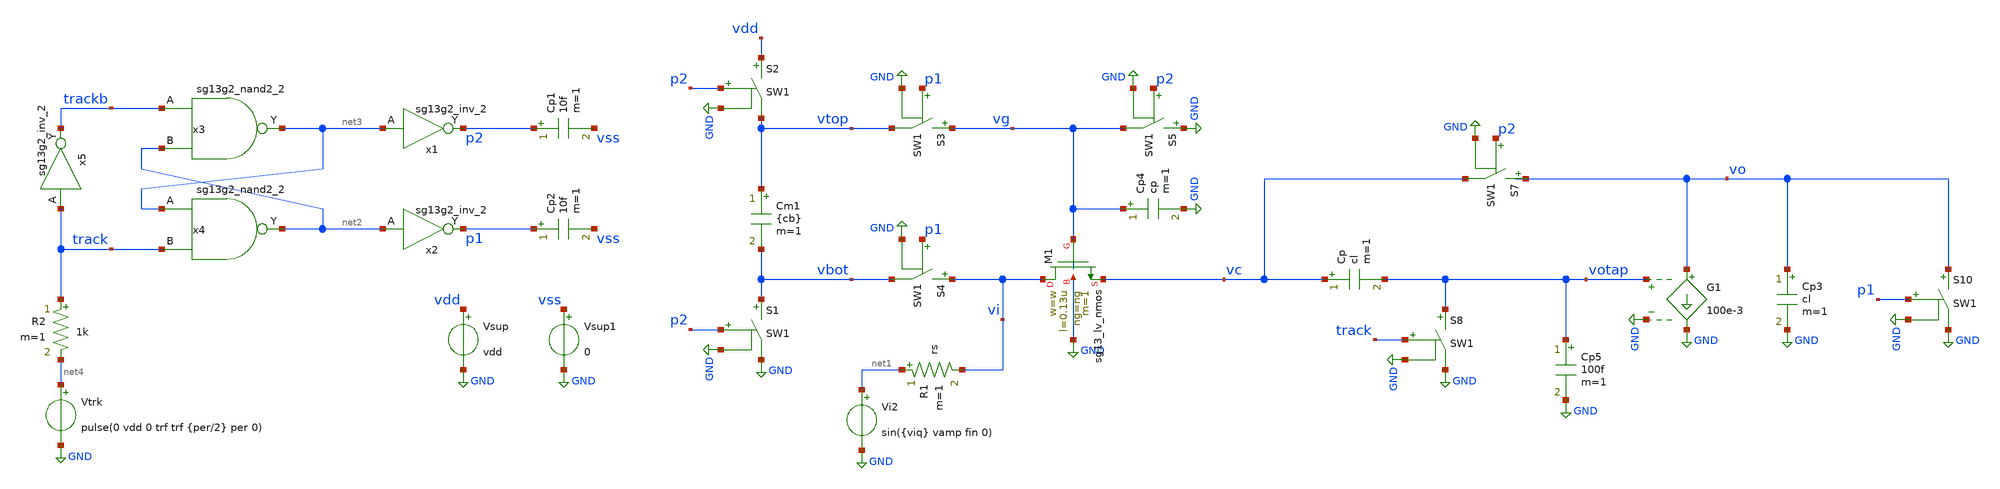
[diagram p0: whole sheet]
** sch_path: xschem/tb_boot_bottom.sch
* IHP-GmbH/IHP-Open-PDK/ihp-sg13g2/libs.tech/xschem/sg13g2_stdcells/sg13g2_inv_2.sch:
* Copyright 2023 IHP PDK Authors
* Licensed under the Apache License, Version 2.0 (the "License");
**.subckt tb_boot_bottom
Cm1 vtop vbot {cb} m=1
S1 vbot GND p2 GND SW1
S2 vdd vtop p2 GND SW1
S3 vg vtop p1 GND SW1
S4 vi vbot p1 GND SW1
S5 GND vg p2 GND SW1
Cp4 vg GND cp m=1
Vi2 net1 GND sin({viq} vamp fin 0)
Cp1 p2 vss 10f m=1
Cp2 p1 vss 10f m=1
x1 p2 net3 VDD VSS sg13g2_inv_2
x2 p1 net2 VDD VSS sg13g2_inv_2
x3 net3 trackb net2 VDD VSS sg13g2_nand2_2
x4 net2 net3 track VDD VSS sg13g2_nand2_2
x5 trackb track VDD VSS sg13g2_inv_2
Vtrk net4 GND pulse(0 vdd 0 trf trf {per/2} per 0)
Vsup vdd GND vdd
Vsup1 vss GND 0
R1 net1 vi rs m=1
XM1 vi vg vc GND sg13_lv_nmos w=w l=0.13u ng=ng m=1 mm_ok=1
Cp vc votap cl m=1
G1 vo GND votap GND 100e-3
S7 vo vc p2 GND SW1
Cp3 vo GND cl m=1
S8 votap GND track GND SW1
S10 vo GND p1 GND SW1
Cp5 votap GND 100f m=1
R2 track net4 1k m=1
**** begin user architecture code


.lib cornerMOSlv.lib mos_tt
.inc /foss/pdks/ihp-sg13g2/libs.ref/sg13g2_stdcell/spice/sg13g2_stdcell.spice
.param vdd=1.2 viq=0.3 vamp=0.2
.param cl=1p cb=1p cp=100f w=100u ng=20
.param ndft=31 npad=5 bin=5 fclk=500e6 runs=15
.param per=1/fclk fin=fclk*bin/ndft trf=100p
.param vh=0 rsw=10 roff=1e9 rs=10

.csparam per=per runs=runs
.csparam tstop1 = 4*per
.csparam tstop2 = per*(ndft+npad)
.option method=gear reltol=1e-6 chgtol=1e-16

.control
    tran 1n $&tstop1
    write tb_boot_bottom.raw
    option numdgt=9
    set wr_singlescale
    set wr_vecnames
    compose bin_vec start=1 stop=$&runs step=1
    foreach i $&bin_vec
      alterparam bin=$i
      reset
      tran 10p $&tstop2 0
      let lin-tstep = per
      let lin-tstart = 1.1n
      linearize
      wrdata tb_boot_bottom_track.txt v(vi) v(vc)
      tran 10p $&tstop2 0
      let lin-tstep = per
      let lin-tstart = 1.9n
      linearize
      wrdata tb_boot_bottom.txt v(vi) v(vo)
      destroy all
      set appendwrite
      unset wr_vecnames
    end
    unset appendwrite
.endc


**** end user architecture code
**.ends

* expanding   symbol:  sg13g2_stdcells/sg13g2_inv_2.sym # of pins=2
** sym_path: sg13g2_stdcells/sg13g2_inv_2.sym
** sch_path: sg13g2_stdcells/sg13g2_inv_2.sch
.subckt sg13g2_inv_2 Y A VDD VSS
*.opin Y
*.ipin A
*.iopin VDD
*.iopin VSS
XM1 Y A VSS VSS sg13_lv_nmos w=1.48u l=130.00n ng=2 m=1 mm_ok=1
XM2 Y A VDD VDD sg13_lv_pmos w=2.24u l=130.00n ng=2 m=1 mm_ok=1
.ends


* expanding   symbol:  sg13g2_stdcells/sg13g2_nand2_2.sym # of pins=3
** sym_path: sg13g2_stdcells/sg13g2_nand2_2.sym
** sch_path: sg13g2_stdcells/sg13g2_nand2_2.sch
.subckt sg13g2_nand2_2 Y A B VDD VSS
*.iopin VDD
*.iopin VSS
*.opin Y
*.ipin B
*.ipin A
XM1 Y A net1 VSS sg13_lv_nmos w=1.44u l=130.00n ng=2 m=1 mm_ok=1
XM2 net1 B VSS VSS sg13_lv_nmos w=1.44u l=130.00n ng=2 m=1 mm_ok=1
XM3 Y A VDD VDD sg13_lv_pmos w=2.24u l=130.00n ng=2 m=1 mm_ok=1
XM4 Y B VDD VDD sg13_lv_pmos w=2.24u l=130.00n ng=2 m=1 mm_ok=1
.ends

.GLOBAL GND
**** begin user architecture code
.MODEL SW1 SW   VT=0.6 VH=vh  RON=rsw ROFF=roff
**** end user architecture code
.end
